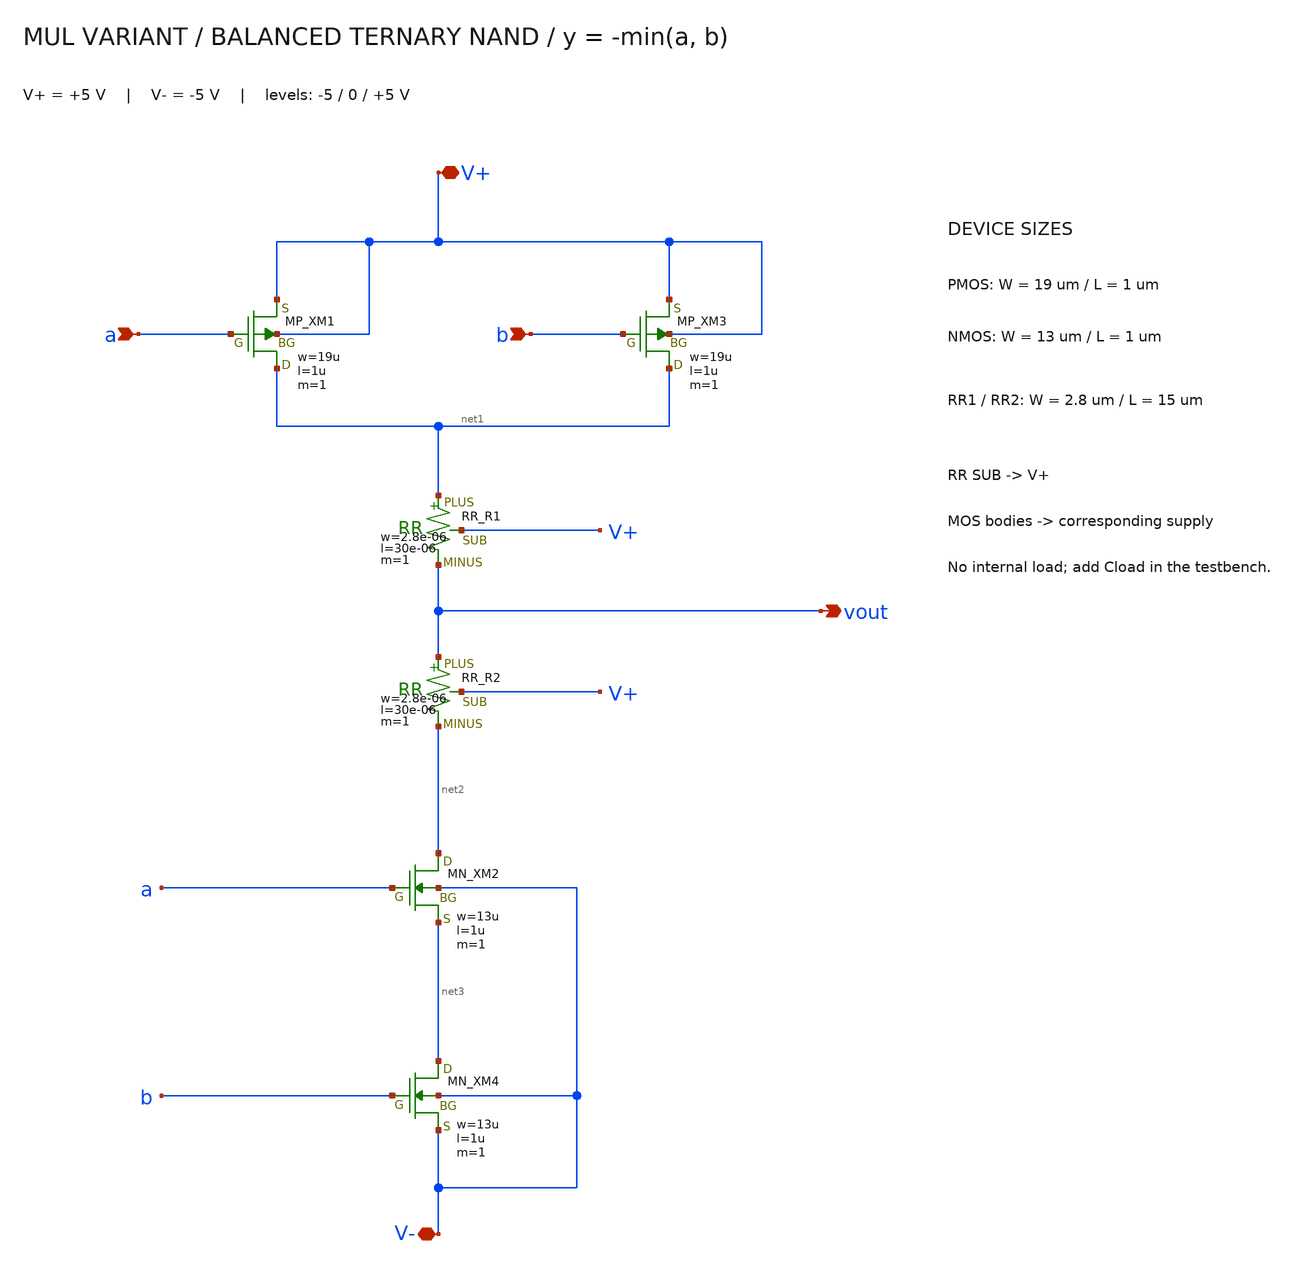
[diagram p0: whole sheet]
** sch_path: member_project/balanced-ternary-logic/PenguinEino/mul_nand.sch
**.subckt mul_nand V+ a b vout V-
*.iopin V+
*.ipin a
*.ipin b
*.opin vout
*.iopin V-
XXM1 net1 a V+ V+ PMOS w=19u l=1u nrd=0 nrs=0 m=1
XXM3 net1 b V+ V+ PMOS w=19u l=1u nrd=0 nrs=0 m=1
XR1 net1 vout V+ F_RR w=2.8e-06 l=30e-06 R=1 tc1=0 tc2=0 m=1
XR2 vout net2 V+ F_RR w=2.8e-06 l=30e-06 R=1 tc1=0 tc2=0 m=1
XXM2 net2 a net3 V- NMOS w=13u l=1u nrd=0 nrs=0 m=1
XXM4 net3 b V- V- NMOS w=13u l=1u nrd=0 nrs=0 m=1
**.ends
.end
